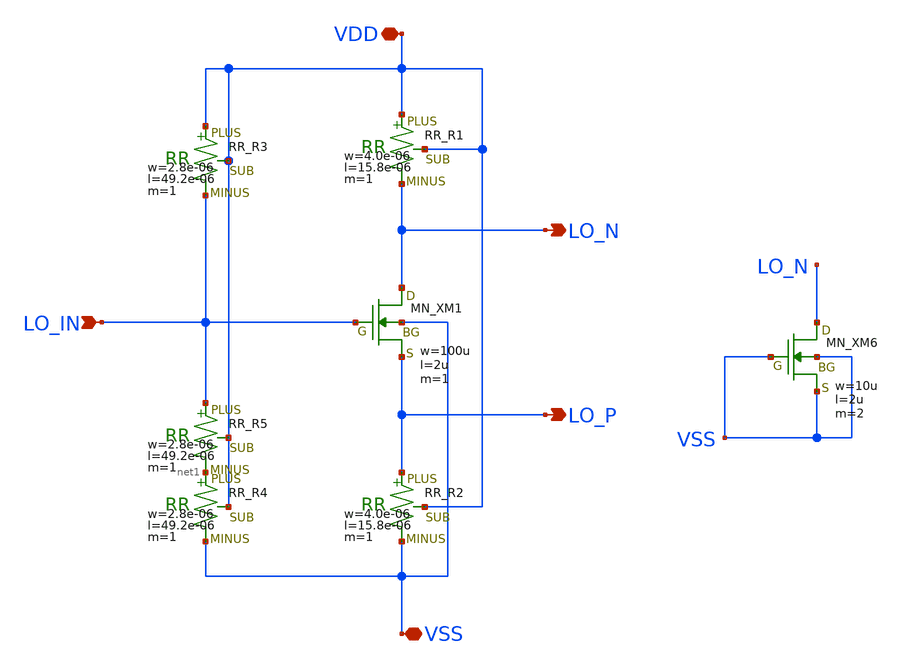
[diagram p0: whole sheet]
** sch_path: member_project/MIXER/noritsuna/xschem/single_to_diff_LO.sch
**.subckt single_to_diff_LO VDD VSS LO_N LO_P LO_IN
*.iopin VDD
*.iopin VSS
*.opin LO_N
*.opin LO_P
*.ipin LO_IN
XXM1 LO_N LO_IN LO_P VSS NMOS w=100u l=2u nrd=0 nrs=0 m=1
XR1 VDD LO_N VDD F_RR w=4.0e-06 l=15.8e-06 R=2.5e+03 tc1=0 tc2=0 m=1
XR2 LO_P VSS VDD F_RR w=4.0e-06 l=15.8e-06 R=2.5e+03 tc1=0 tc2=0 m=1
XR3 VDD LO_IN VDD F_RR w=2.8e-06 l=49.2e-06 R=20e+03 tc1=0 tc2=0 m=1
XR4 net1 VSS VDD F_RR w=2.8e-06 l=49.2e-06 R=40e+03 tc1=0 tc2=0 m=1
XXM6 LO_N VSS VSS VSS NMOS w=10u l=2u nrd=0 nrs=0 m=2
XR5 LO_IN net1 VDD F_RR w=2.8e-06 l=49.2e-06 R=40e+03 tc1=0 tc2=0 m=1
**.ends
.end
